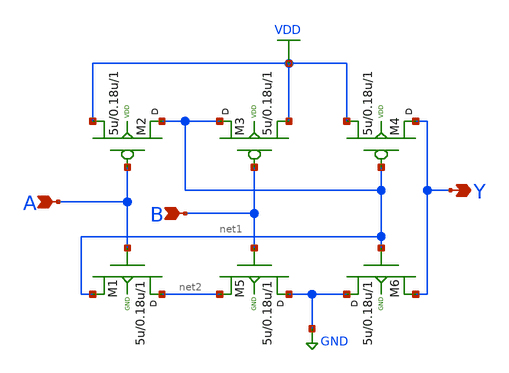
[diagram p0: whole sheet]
** sch_path: sch/AND2_1.sch
**.subckt AND2_1 A B Y
*.ipin A
*.ipin B
*.opin Y
M1 net2 A net1 GND nfet w=5u l=0.18u m=1
M2 net1 A VDD VDD pfet w=5u l=0.18u m=1
M3 net1 B VDD VDD pfet w=5u l=0.18u m=1
M4 Y net1 VDD VDD pfet w=5u l=0.18u m=1
M5 GND B net2 GND nfet w=5u l=0.18u m=1
M6 GND net1 Y GND nfet w=5u l=0.18u m=1
**.ends
.GLOBAL GND
.GLOBAL VDD
.end
